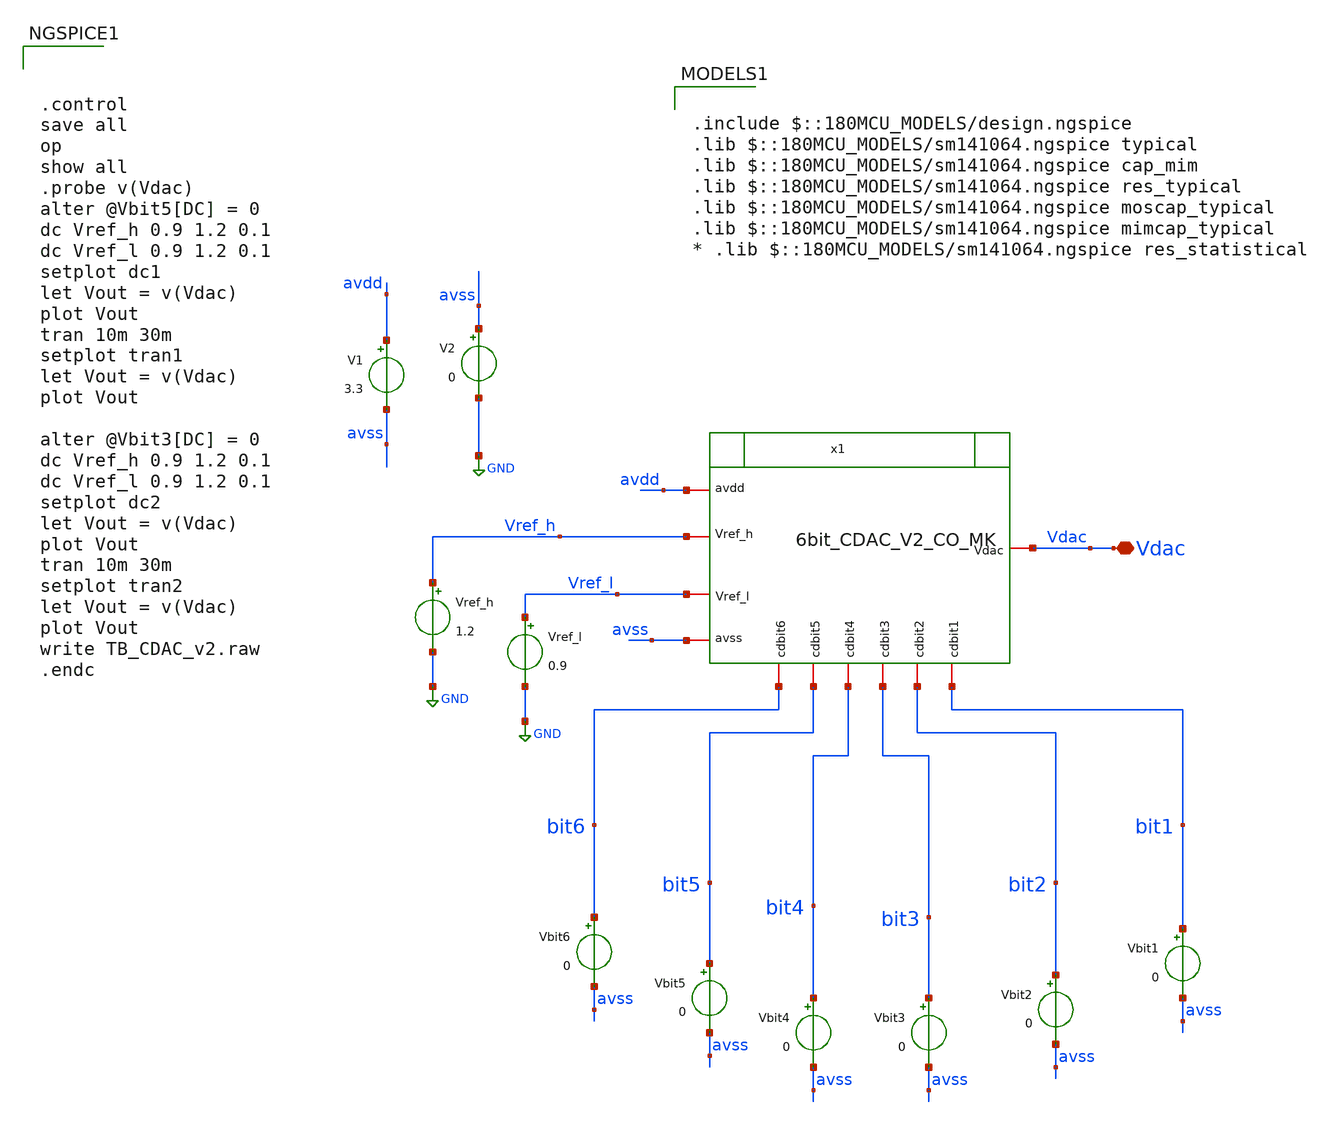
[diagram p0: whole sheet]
** sch_path: designs/libs/WK_Kadam/TB_6bit_CDAC_CO_V1_MK.sch
**.subckt TB_6bit_CDAC_CO_V1_MK Vdac
*.iopin Vdac
V1 avdd avss 3.3
V2 avss GND 0
Vbit1 bit1 avss 0
Vbit2 bit2 avss 0
Vbit3 bit3 avss 0
Vbit4 bit4 avss 0
Vbit5 bit5 avss 0
Vbit6 bit6 avss 0
Vref_h Vref_h GND 1.2
Vref_l Vref_l GND 0.9
x1 Vref_l Vdac avdd avss Vref_h bit6 bit5 bit3 bit1 bit2 bit4 6bit_CDAC_V2_CO_MK
**** begin user architecture code



.control
save all
op
show all
.probe v(Vdac)
alter @Vbit5[DC] = 0
dc Vref_h 0.9 1.2 0.1
dc Vref_l 0.9 1.2 0.1
setplot dc1
let Vout = v(Vdac)
plot Vout
tran 10m 30m
setplot tran1
let Vout = v(Vdac)
plot Vout

alter @Vbit3[DC] = 0
dc Vref_h 0.9 1.2 0.1
dc Vref_l 0.9 1.2 0.1
setplot dc2
let Vout = v(Vdac)
plot Vout
tran 10m 30m
setplot tran2
let Vout = v(Vdac)
plot Vout
write TB_CDAC_v2.raw
.endc



.include $::180MCU_MODELS/design.ngspice
.lib $::180MCU_MODELS/sm141064.ngspice typical
.lib $::180MCU_MODELS/sm141064.ngspice cap_mim
.lib $::180MCU_MODELS/sm141064.ngspice res_typical
.lib $::180MCU_MODELS/sm141064.ngspice moscap_typical
.lib $::180MCU_MODELS/sm141064.ngspice mimcap_typical
* .lib $::180MCU_MODELS/sm141064.ngspice res_statistical

**** end user architecture code
**.ends

* expanding   symbol:  libs/WK_Kadam/6bit_CDAC_V2_CO_MK.sym # of pins=11
** sym_path: designs/libs/WK_Kadam/6bit_CDAC_V2_CO_MK.sym
** sch_path: designs/libs/WK_Kadam/6bit_CDAC_V2_CO_MK.sch
.subckt 6bit_CDAC_V2_CO_MK Vref_l Vdac avdd avss Vref_h cdbit6 cdbit5 cdbit3 cdbit1 cdbit2 cdbit4
*.iopin Vref_h
*.iopin Vdac
*.iopin avdd
*.iopin avss
*.iopin cdbit6
*.iopin cdbit5
*.iopin cdbit4
*.iopin cdbit3
*.iopin cdbit2
*.iopin cdbit1
*.iopin Vref_l
XC3 Vdac net2 cap_mim_2f0_m3m4_noshield c_width=10e-6 c_length=10e-6 m=4
XC4 Vdac net3 cap_mim_2f0_m3m4_noshield c_width=10e-6 c_length=10e-6 m=8
XC5 Vdac net4 cap_mim_2f0_m3m4_noshield c_width=10e-6 c_length=10e-6 m=16
XC6 Vdac net5 cap_mim_2f0_m3m4_noshield c_width=10e-6 c_length=10e-6 m=32
XC7 Vdac net6 cap_mim_2f0_m3m4_noshield c_width=10e-6 c_length=10e-6 m=64
XC1 Vdac avss cap_mim_2f0_m3m4_noshield c_width=10e-6 c_length=10e-6 m=2
XC2 Vdac net1 cap_mim_2f0_m3m4_noshield c_width=10e-6 c_length=10e-6 m=2
x1 net6 cdbit6 avss avdd Vref_h Vref_l c_dac2_switch
x2 net5 cdbit5 avss avdd Vref_h Vref_l c_dac2_switch
x3 net4 cdbit4 avss avdd Vref_h Vref_l c_dac2_switch
x4 net3 cdbit3 avss avdd Vref_h Vref_l c_dac2_switch
x5 net2 cdbit2 avss avdd Vref_h Vref_l c_dac2_switch
x6 net1 cdbit1 avss avdd Vref_h Vref_l c_dac2_switch
.ends


* expanding   symbol:  libs/WK_Kadam/c_dac2_switch.sym # of pins=6
** sym_path: designs/libs/WK_Kadam/c_dac2_switch.sym
** sch_path: designs/libs/WK_Kadam/c_dac2_switch.sch
.subckt c_dac2_switch sw_vout sw_bit avss avdd sw_Vref vreflow
*.iopin avdd
*.iopin avss
*.iopin sw_bit
*.iopin sw_vout
*.iopin sw_Vref
*.iopin vreflow
XM1 sw_vout sw_bit sw_Vref avss nfet_03v3 L=0.28u W=2u nf=1 ad='int((nf+1)/2) * W/nf * 0.18u' as='int((nf+2)/2) * W/nf * 0.18u'
+ pd='2*int((nf+1)/2) * (W/nf + 0.18u)' ps='2*int((nf+2)/2) * (W/nf + 0.18u)' nrd='0.18u / W' nrs='0.18u / W'
+ sa=0 sb=0 sd=0 m=1
XM3 sw_vout net1 vreflow avss nfet_03v3 L=0.28u W=2u nf=1 ad='int((nf+1)/2) * W/nf * 0.18u' as='int((nf+2)/2) * W/nf * 0.18u'
+ pd='2*int((nf+1)/2) * (W/nf + 0.18u)' ps='2*int((nf+2)/2) * (W/nf + 0.18u)' nrd='0.18u / W' nrs='0.18u / W'
+ sa=0 sb=0 sd=0 m=1
XM4 vreflow sw_bit sw_vout avdd pfet_03v3 L=0.28u W=2u nf=1 ad='int((nf+1)/2) * W/nf * 0.18u' as='int((nf+2)/2) * W/nf * 0.18u'
+ pd='2*int((nf+1)/2) * (W/nf + 0.18u)' ps='2*int((nf+2)/2) * (W/nf + 0.18u)' nrd='0.18u / W' nrs='0.18u / W'
+ sa=0 sb=0 sd=0 m=1
XM2 sw_Vref net1 sw_vout avdd pfet_03v3 L=0.28u W=2u nf=1 ad='int((nf+1)/2) * W/nf * 0.18u' as='int((nf+2)/2) * W/nf * 0.18u'
+ pd='2*int((nf+1)/2) * (W/nf + 0.18u)' ps='2*int((nf+2)/2) * (W/nf + 0.18u)' nrd='0.18u / W' nrs='0.18u / W'
+ sa=0 sb=0 sd=0 m=1
x1v avdd sw_bit net1 avss inv_test
.ends


* expanding   symbol:  libs/WK_Kadam/inv_test.sym # of pins=4
** sym_path: libs/WK_Kadam/inv_test.sym
** sch_path: libs/WK_Kadam/inv_test.sch
.subckt inv_test avdd in out avss
*.iopin avdd
*.iopin avss
*.iopin in
*.iopin out
XM3 out in avss avss nfet_03v3 L=0.28u W=1u nf=1 ad='int((nf+1)/2) * W/nf * 0.18u' as='int((nf+2)/2) * W/nf * 0.18u'
+ pd='2*int((nf+1)/2) * (W/nf + 0.18u)' ps='2*int((nf+2)/2) * (W/nf + 0.18u)' nrd='0.18u / W' nrs='0.18u / W'
+ sa=0 sb=0 sd=0 m=1
XM4 out in avdd avdd pfet_03v3 L=0.28u W=2.5u nf=1 ad='int((nf+1)/2) * W/nf * 0.18u' as='int((nf+2)/2) * W/nf * 0.18u'
+ pd='2*int((nf+1)/2) * (W/nf + 0.18u)' ps='2*int((nf+2)/2) * (W/nf + 0.18u)' nrd='0.18u / W' nrs='0.18u / W'
+ sa=0 sb=0 sd=0 m=1
.ends

.GLOBAL GND
.end
